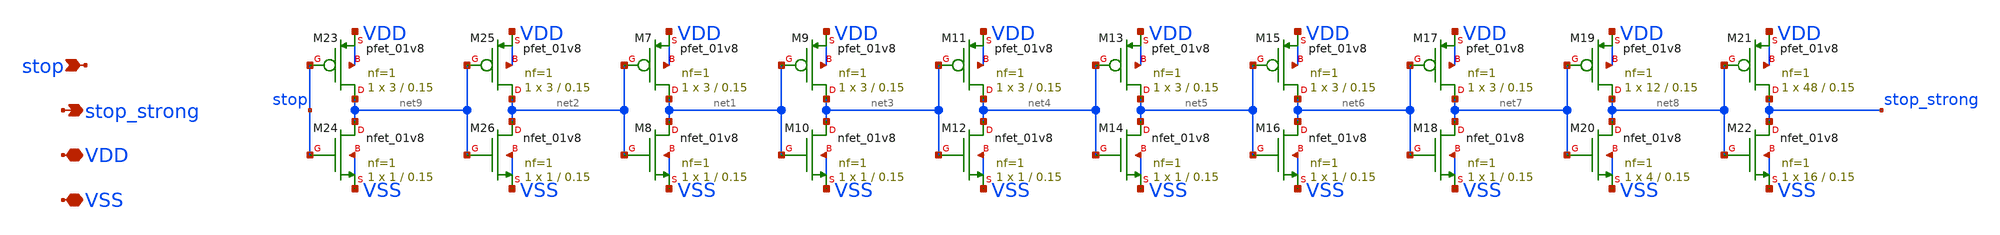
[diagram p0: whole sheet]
** sch_path: xschem/stop_buffer.sch
**.subckt stop_buffer VDD VSS stop stop_strong
*.iopin VDD
*.iopin VSS
*.ipin stop
*.opin stop_strong
XM7 net1 net2 VDD VDD sky130_fd_pr__pfet_01v8 L=0.15 W=3 nf=1 ad='int((nf+1)/2) * W/nf * 0.29' as='int((nf+2)/2) * W/nf * 0.29'
+ pd='2*int((nf+1)/2) * (W/nf + 0.29)' ps='2*int((nf+2)/2) * (W/nf + 0.29)' nrd='0.29 / W' nrs='0.29 / W'
+ sa=0 sb=0 sd=0 mult=1 m=1
XM8 net1 net2 VSS VSS sky130_fd_pr__nfet_01v8 L=0.15 W=1 nf=1 ad='int((nf+1)/2) * W/nf * 0.29' as='int((nf+2)/2) * W/nf * 0.29'
+ pd='2*int((nf+1)/2) * (W/nf + 0.29)' ps='2*int((nf+2)/2) * (W/nf + 0.29)' nrd='0.29 / W' nrs='0.29 / W'
+ sa=0 sb=0 sd=0 mult=1 m=1
XM9 net3 net1 VDD VDD sky130_fd_pr__pfet_01v8 L=0.15 W=3 nf=1 ad='int((nf+1)/2) * W/nf * 0.29' as='int((nf+2)/2) * W/nf * 0.29'
+ pd='2*int((nf+1)/2) * (W/nf + 0.29)' ps='2*int((nf+2)/2) * (W/nf + 0.29)' nrd='0.29 / W' nrs='0.29 / W'
+ sa=0 sb=0 sd=0 mult=1 m=1
XM10 net3 net1 VSS VSS sky130_fd_pr__nfet_01v8 L=0.15 W=1 nf=1 ad='int((nf+1)/2) * W/nf * 0.29' as='int((nf+2)/2) * W/nf * 0.29'
+ pd='2*int((nf+1)/2) * (W/nf + 0.29)' ps='2*int((nf+2)/2) * (W/nf + 0.29)' nrd='0.29 / W' nrs='0.29 / W'
+ sa=0 sb=0 sd=0 mult=1 m=1
XM11 net4 net3 VDD VDD sky130_fd_pr__pfet_01v8 L=0.15 W=3 nf=1 ad='int((nf+1)/2) * W/nf * 0.29' as='int((nf+2)/2) * W/nf * 0.29'
+ pd='2*int((nf+1)/2) * (W/nf + 0.29)' ps='2*int((nf+2)/2) * (W/nf + 0.29)' nrd='0.29 / W' nrs='0.29 / W'
+ sa=0 sb=0 sd=0 mult=1 m=1
XM12 net4 net3 VSS VSS sky130_fd_pr__nfet_01v8 L=0.15 W=1 nf=1 ad='int((nf+1)/2) * W/nf * 0.29' as='int((nf+2)/2) * W/nf * 0.29'
+ pd='2*int((nf+1)/2) * (W/nf + 0.29)' ps='2*int((nf+2)/2) * (W/nf + 0.29)' nrd='0.29 / W' nrs='0.29 / W'
+ sa=0 sb=0 sd=0 mult=1 m=1
XM13 net5 net4 VDD VDD sky130_fd_pr__pfet_01v8 L=0.15 W=3 nf=1 ad='int((nf+1)/2) * W/nf * 0.29' as='int((nf+2)/2) * W/nf * 0.29'
+ pd='2*int((nf+1)/2) * (W/nf + 0.29)' ps='2*int((nf+2)/2) * (W/nf + 0.29)' nrd='0.29 / W' nrs='0.29 / W'
+ sa=0 sb=0 sd=0 mult=1 m=1
XM14 net5 net4 VSS VSS sky130_fd_pr__nfet_01v8 L=0.15 W=1 nf=1 ad='int((nf+1)/2) * W/nf * 0.29' as='int((nf+2)/2) * W/nf * 0.29'
+ pd='2*int((nf+1)/2) * (W/nf + 0.29)' ps='2*int((nf+2)/2) * (W/nf + 0.29)' nrd='0.29 / W' nrs='0.29 / W'
+ sa=0 sb=0 sd=0 mult=1 m=1
XM15 net6 net5 VDD VDD sky130_fd_pr__pfet_01v8 L=0.15 W=3 nf=1 ad='int((nf+1)/2) * W/nf * 0.29' as='int((nf+2)/2) * W/nf * 0.29'
+ pd='2*int((nf+1)/2) * (W/nf + 0.29)' ps='2*int((nf+2)/2) * (W/nf + 0.29)' nrd='0.29 / W' nrs='0.29 / W'
+ sa=0 sb=0 sd=0 mult=1 m=1
XM16 net6 net5 VSS VSS sky130_fd_pr__nfet_01v8 L=0.15 W=1 nf=1 ad='int((nf+1)/2) * W/nf * 0.29' as='int((nf+2)/2) * W/nf * 0.29'
+ pd='2*int((nf+1)/2) * (W/nf + 0.29)' ps='2*int((nf+2)/2) * (W/nf + 0.29)' nrd='0.29 / W' nrs='0.29 / W'
+ sa=0 sb=0 sd=0 mult=1 m=1
XM17 net7 net6 VDD VDD sky130_fd_pr__pfet_01v8 L=0.15 W=3 nf=1 ad='int((nf+1)/2) * W/nf * 0.29' as='int((nf+2)/2) * W/nf * 0.29'
+ pd='2*int((nf+1)/2) * (W/nf + 0.29)' ps='2*int((nf+2)/2) * (W/nf + 0.29)' nrd='0.29 / W' nrs='0.29 / W'
+ sa=0 sb=0 sd=0 mult=1 m=1
XM18 net7 net6 VSS VSS sky130_fd_pr__nfet_01v8 L=0.15 W=1 nf=1 ad='int((nf+1)/2) * W/nf * 0.29' as='int((nf+2)/2) * W/nf * 0.29'
+ pd='2*int((nf+1)/2) * (W/nf + 0.29)' ps='2*int((nf+2)/2) * (W/nf + 0.29)' nrd='0.29 / W' nrs='0.29 / W'
+ sa=0 sb=0 sd=0 mult=1 m=1
XM19 net8 net7 VDD VDD sky130_fd_pr__pfet_01v8 L=0.15 W=12 nf=1 ad='int((nf+1)/2) * W/nf * 0.29' as='int((nf+2)/2) * W/nf * 0.29'
+ pd='2*int((nf+1)/2) * (W/nf + 0.29)' ps='2*int((nf+2)/2) * (W/nf + 0.29)' nrd='0.29 / W' nrs='0.29 / W'
+ sa=0 sb=0 sd=0 mult=1 m=1
XM20 net8 net7 VSS VSS sky130_fd_pr__nfet_01v8 L=0.15 W=4 nf=1 ad='int((nf+1)/2) * W/nf * 0.29' as='int((nf+2)/2) * W/nf * 0.29'
+ pd='2*int((nf+1)/2) * (W/nf + 0.29)' ps='2*int((nf+2)/2) * (W/nf + 0.29)' nrd='0.29 / W' nrs='0.29 / W'
+ sa=0 sb=0 sd=0 mult=1 m=1
XM21 stop_strong net8 VDD VDD sky130_fd_pr__pfet_01v8 L=0.15 W=48 nf=1 ad='int((nf+1)/2) * W/nf * 0.29'
+ as='int((nf+2)/2) * W/nf * 0.29' pd='2*int((nf+1)/2) * (W/nf + 0.29)' ps='2*int((nf+2)/2) * (W/nf + 0.29)'
+ nrd='0.29 / W' nrs='0.29 / W' sa=0 sb=0 sd=0 mult=1 m=1
XM22 stop_strong net8 VSS VSS sky130_fd_pr__nfet_01v8 L=0.15 W=16 nf=1 ad='int((nf+1)/2) * W/nf * 0.29'
+ as='int((nf+2)/2) * W/nf * 0.29' pd='2*int((nf+1)/2) * (W/nf + 0.29)' ps='2*int((nf+2)/2) * (W/nf + 0.29)'
+ nrd='0.29 / W' nrs='0.29 / W' sa=0 sb=0 sd=0 mult=1 m=1
XM23 net9 stop VDD VDD sky130_fd_pr__pfet_01v8 L=0.15 W=3 nf=1 ad='int((nf+1)/2) * W/nf * 0.29' as='int((nf+2)/2) * W/nf * 0.29'
+ pd='2*int((nf+1)/2) * (W/nf + 0.29)' ps='2*int((nf+2)/2) * (W/nf + 0.29)' nrd='0.29 / W' nrs='0.29 / W'
+ sa=0 sb=0 sd=0 mult=1 m=1
XM24 net9 stop VSS VSS sky130_fd_pr__nfet_01v8 L=0.15 W=1 nf=1 ad='int((nf+1)/2) * W/nf * 0.29' as='int((nf+2)/2) * W/nf * 0.29'
+ pd='2*int((nf+1)/2) * (W/nf + 0.29)' ps='2*int((nf+2)/2) * (W/nf + 0.29)' nrd='0.29 / W' nrs='0.29 / W'
+ sa=0 sb=0 sd=0 mult=1 m=1
XM25 net2 net9 VDD VDD sky130_fd_pr__pfet_01v8 L=0.15 W=3 nf=1 ad='int((nf+1)/2) * W/nf * 0.29' as='int((nf+2)/2) * W/nf * 0.29'
+ pd='2*int((nf+1)/2) * (W/nf + 0.29)' ps='2*int((nf+2)/2) * (W/nf + 0.29)' nrd='0.29 / W' nrs='0.29 / W'
+ sa=0 sb=0 sd=0 mult=1 m=1
XM26 net2 net9 VSS VSS sky130_fd_pr__nfet_01v8 L=0.15 W=1 nf=1 ad='int((nf+1)/2) * W/nf * 0.29' as='int((nf+2)/2) * W/nf * 0.29'
+ pd='2*int((nf+1)/2) * (W/nf + 0.29)' ps='2*int((nf+2)/2) * (W/nf + 0.29)' nrd='0.29 / W' nrs='0.29 / W'
+ sa=0 sb=0 sd=0 mult=1 m=1
**.ends
.end
